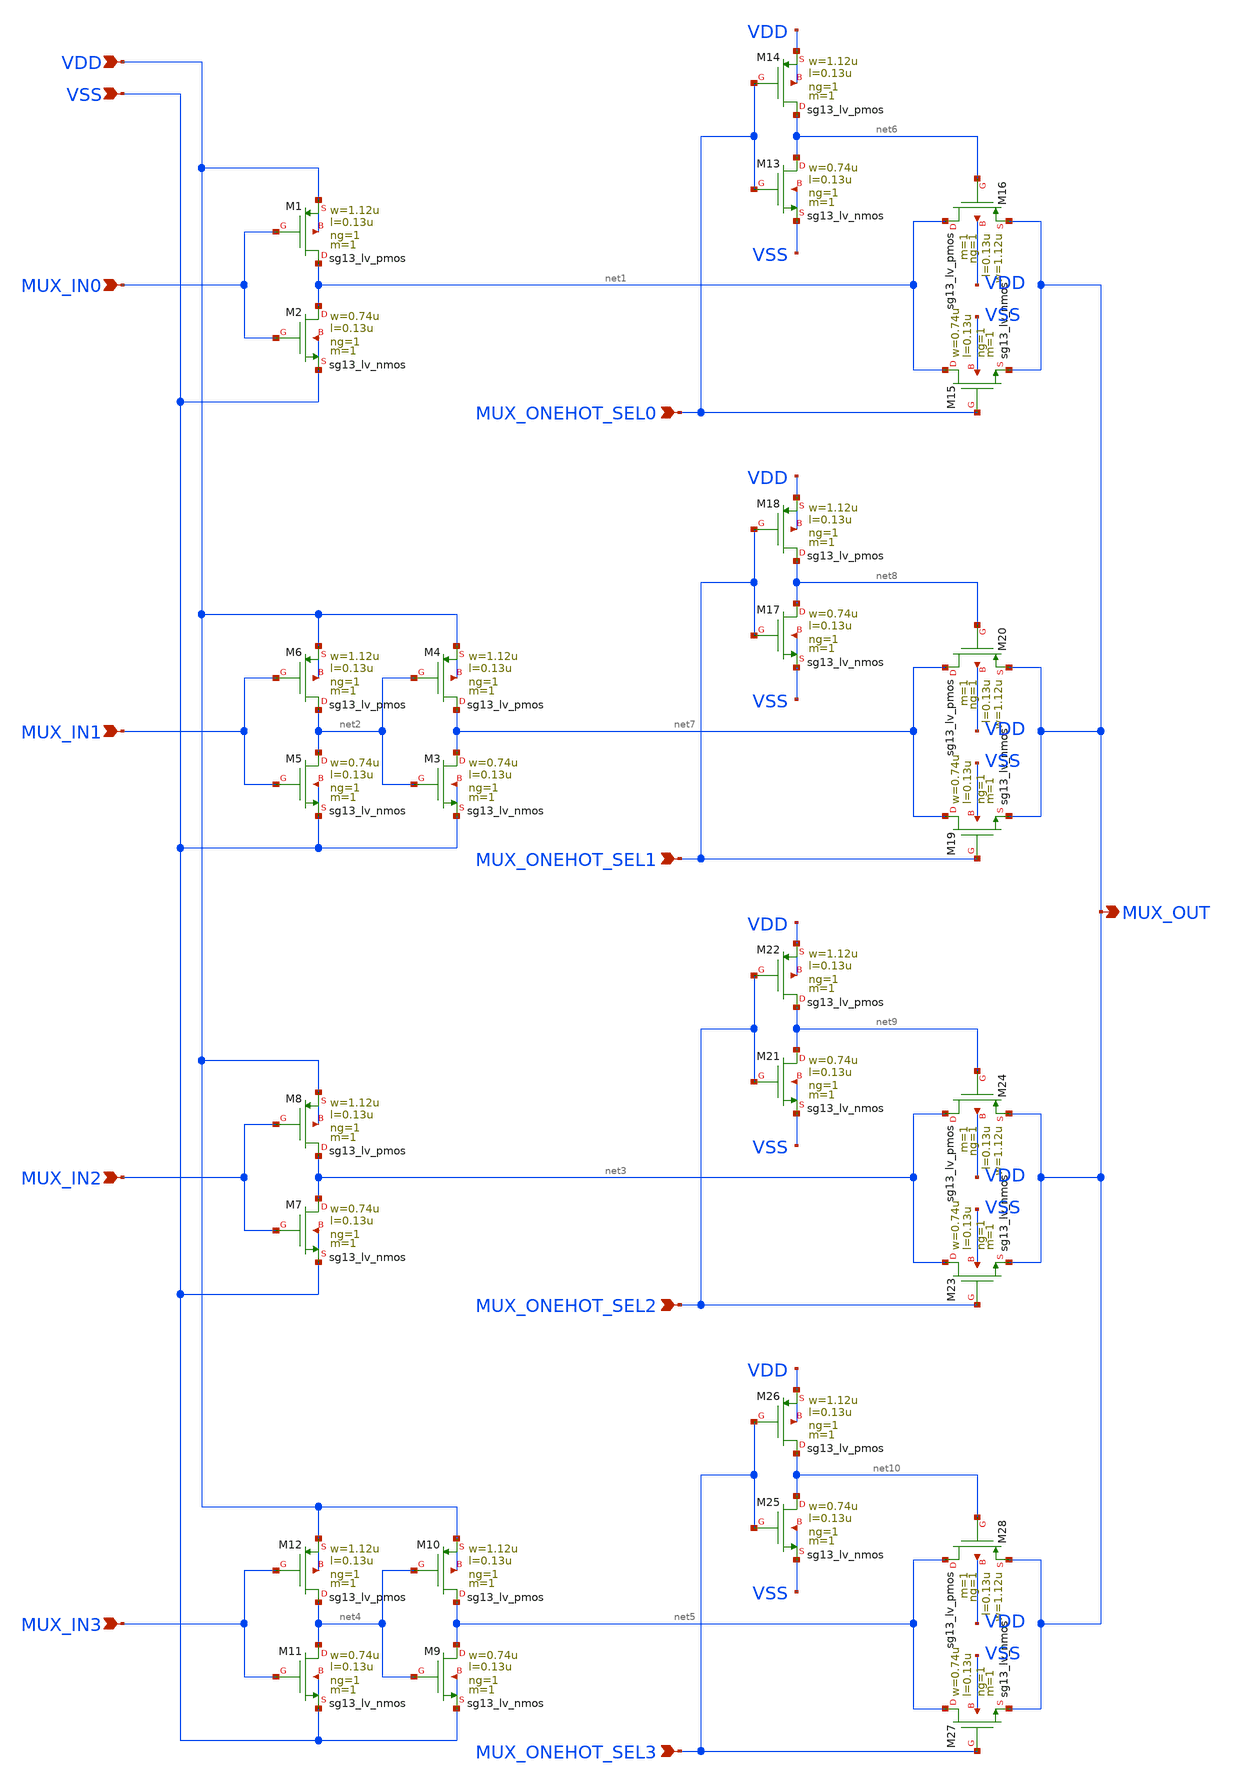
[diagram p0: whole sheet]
** sch_path: schematics/hx_mux_4to1_leaf.sch
**.subckt hx_mux_4to1_leaf VDD VSS MUX_IN0 MUX_OUT MUX_ONEHOT_SEL0 MUX_IN1 MUX_IN2 MUX_IN3
*+ MUX_ONEHOT_SEL1 MUX_ONEHOT_SEL2 MUX_ONEHOT_SEL3
*.ipin VDD
*.ipin VSS
*.ipin MUX_IN0
*.opin MUX_OUT
*.ipin MUX_ONEHOT_SEL0
*.ipin MUX_IN1
*.ipin MUX_IN2
*.ipin MUX_IN3
*.ipin MUX_ONEHOT_SEL1
*.ipin MUX_ONEHOT_SEL2
*.ipin MUX_ONEHOT_SEL3
XM2 net1 MUX_IN0 VSS VSS sg13_lv_nmos w=0.74u l=0.13u ng=1 m=1 mm_ok=1
XM1 net1 MUX_IN0 VDD VDD sg13_lv_pmos w=1.12u l=0.13u ng=1 m=1 mm_ok=1
XM3 net7 net2 VSS VSS sg13_lv_nmos w=0.74u l=0.13u ng=1 m=1 mm_ok=1
XM4 net7 net2 VDD VDD sg13_lv_pmos w=1.12u l=0.13u ng=1 m=1 mm_ok=1
XM5 net2 MUX_IN1 VSS VSS sg13_lv_nmos w=0.74u l=0.13u ng=1 m=1 mm_ok=1
XM6 net2 MUX_IN1 VDD VDD sg13_lv_pmos w=1.12u l=0.13u ng=1 m=1 mm_ok=1
XM7 net3 MUX_IN2 VSS VSS sg13_lv_nmos w=0.74u l=0.13u ng=1 m=1 mm_ok=1
XM8 net3 MUX_IN2 VDD VDD sg13_lv_pmos w=1.12u l=0.13u ng=1 m=1 mm_ok=1
XM9 net5 net4 VSS VSS sg13_lv_nmos w=0.74u l=0.13u ng=1 m=1 mm_ok=1
XM10 net5 net4 VDD VDD sg13_lv_pmos w=1.12u l=0.13u ng=1 m=1 mm_ok=1
XM11 net4 MUX_IN3 VSS VSS sg13_lv_nmos w=0.74u l=0.13u ng=1 m=1 mm_ok=1
XM12 net4 MUX_IN3 VDD VDD sg13_lv_pmos w=1.12u l=0.13u ng=1 m=1 mm_ok=1
XM13 net6 MUX_ONEHOT_SEL0 VSS VSS sg13_lv_nmos w=0.74u l=0.13u ng=1 m=1 mm_ok=1
XM14 net6 MUX_ONEHOT_SEL0 VDD VDD sg13_lv_pmos w=1.12u l=0.13u ng=1 m=1 mm_ok=1
XM15 net1 MUX_ONEHOT_SEL0 MUX_OUT VSS sg13_lv_nmos w=0.74u l=0.13u ng=1 m=1 mm_ok=1
XM16 net1 net6 MUX_OUT VDD sg13_lv_pmos w=1.12u l=0.13u ng=1 m=1 mm_ok=1
XM17 net8 MUX_ONEHOT_SEL1 VSS VSS sg13_lv_nmos w=0.74u l=0.13u ng=1 m=1 mm_ok=1
XM18 net8 MUX_ONEHOT_SEL1 VDD VDD sg13_lv_pmos w=1.12u l=0.13u ng=1 m=1 mm_ok=1
XM19 net7 MUX_ONEHOT_SEL1 MUX_OUT VSS sg13_lv_nmos w=0.74u l=0.13u ng=1 m=1 mm_ok=1
XM20 net7 net8 MUX_OUT VDD sg13_lv_pmos w=1.12u l=0.13u ng=1 m=1 mm_ok=1
XM21 net9 MUX_ONEHOT_SEL2 VSS VSS sg13_lv_nmos w=0.74u l=0.13u ng=1 m=1 mm_ok=1
XM22 net9 MUX_ONEHOT_SEL2 VDD VDD sg13_lv_pmos w=1.12u l=0.13u ng=1 m=1 mm_ok=1
XM23 net3 MUX_ONEHOT_SEL2 MUX_OUT VSS sg13_lv_nmos w=0.74u l=0.13u ng=1 m=1 mm_ok=1
XM24 net3 net9 MUX_OUT VDD sg13_lv_pmos w=1.12u l=0.13u ng=1 m=1 mm_ok=1
XM25 net10 MUX_ONEHOT_SEL3 VSS VSS sg13_lv_nmos w=0.74u l=0.13u ng=1 m=1 mm_ok=1
XM26 net10 MUX_ONEHOT_SEL3 VDD VDD sg13_lv_pmos w=1.12u l=0.13u ng=1 m=1 mm_ok=1
XM27 net5 MUX_ONEHOT_SEL3 MUX_OUT VSS sg13_lv_nmos w=0.74u l=0.13u ng=1 m=1 mm_ok=1
XM28 net5 net10 MUX_OUT VDD sg13_lv_pmos w=1.12u l=0.13u ng=1 m=1 mm_ok=1
**.ends
.end
